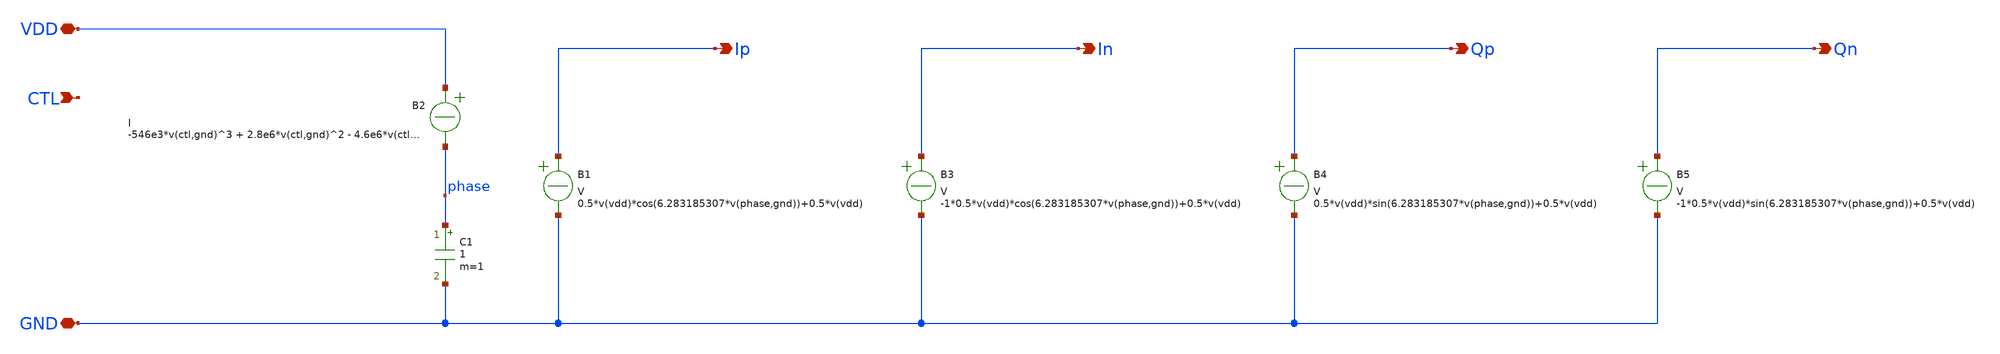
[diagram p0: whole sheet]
** sch_path: design/vco_2-4GHz/vco_2-4GHz_behavourial.sch
**.subckt vco_2-4GHz_behavourial CTL VDD GND Ip In Qp Qn
*.ipin CTL
*.iopin VDD
*.iopin GND
*.opin Ip
*.opin In
*.opin Qp
*.opin Qn
C1 phase GND 1 m=1
B2 VDD phase I = -546e3*v(ctl,gnd)^3 + 2.8e6*v(ctl,gnd)^2 - 4.6e6*v(ctl,gnd) + 5.65e6
B1 Ip GND V = 0.5*v(vdd)*cos(6.283185307*v(phase,gnd))+0.5*v(vdd)
B3 In GND V = -1*0.5*v(vdd)*cos(6.283185307*v(phase,gnd))+0.5*v(vdd)
B4 Qp GND V = 0.5*v(vdd)*sin(6.283185307*v(phase,gnd))+0.5*v(vdd)
B5 Qn GND V = -1*0.5*v(vdd)*sin(6.283185307*v(phase,gnd))+0.5*v(vdd)
**.ends
.end
